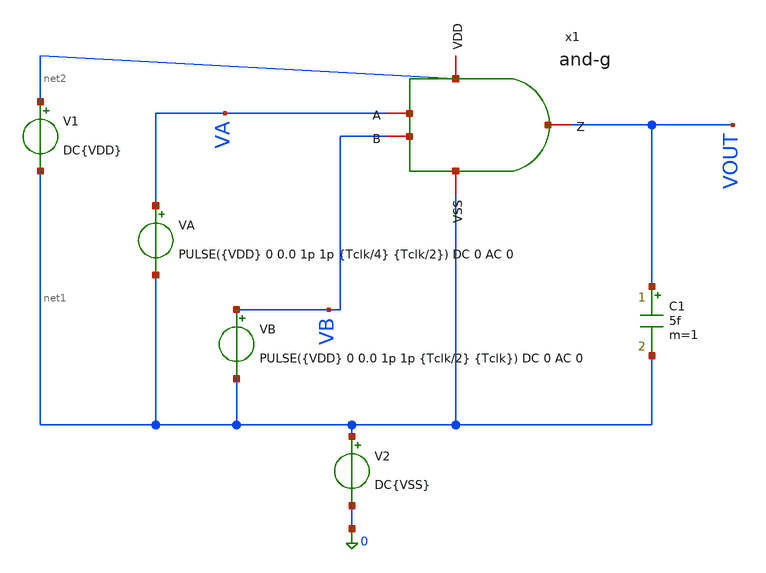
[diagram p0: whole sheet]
** sch_path: verification/testbenches/tb_and-g.sch
**.subckt tb_and-g
x1 net2 VA VB VOUT net1 and-g
VA VA net1 PULSE({VDD} 0 0.0 1p 1p {Tclk/4} {Tclk/2}) DC 0 AC 0
V1 net2 net1 DC{VDD}
VB VB net1 PULSE({VDD} 0 0.0 1p 1p {Tclk/2} {Tclk}) DC 0 AC 0
V2 net1 0 DC{VSS}
C1 VOUT net1 5f m=1
**** begin user architecture code


* Circuit Parameters
.param VDD = 1.2
.param VSS = 0.0
.param Tclk = 10n
.options TEMP = 27.0
* Include Models - IHP SG13G2
.lib cornerMOSlv.lib mos_tt
* OP Parameters & Singals to save
.save all
*Simulations
.control
tran 0.01u 100n
setplot tran1
plot v(VA) v(VB)+1.5 v(VOUT)+3
set filetype = ascii
write dcsweep.raw
.endc
.end


**** end user architecture code
**.ends

* expanding   symbol:  blocks/and-g/and-g.sym # of pins=5
** sym_path: blocks/and-g/and-g.sym
** sch_path: blocks/and-g/and-g.sch
.subckt and-g VDD A B Z VSS
*.iopin VDD
*.iopin Z
*.iopin A
*.iopin B
*.iopin VSS
XM0 VDD A net1 VDD sg13_lv_pmos w=1.15u l=0.15u ng=1 m=1 mm_ok=1
XM1 VDD B net1 VDD sg13_lv_pmos w=1.15u l=0.15u ng=1 m=1 mm_ok=1
XM4 VDD net1 Z VDD sg13_lv_pmos w=1.15u l=0.15u ng=1 m=1 mm_ok=1
XM6 Z net1 VSS VSS sg13_lv_nmos w=0.75u l=0.15u ng=1 m=1 mm_ok=1
XM2 net1 A net2 VSS sg13_lv_nmos w=1.15u l=0.15u ng=1 m=1 mm_ok=1
XM3 net2 B VSS VSS sg13_lv_nmos w=1.15u l=0.15u ng=1 m=1 mm_ok=1
.ends

.end
